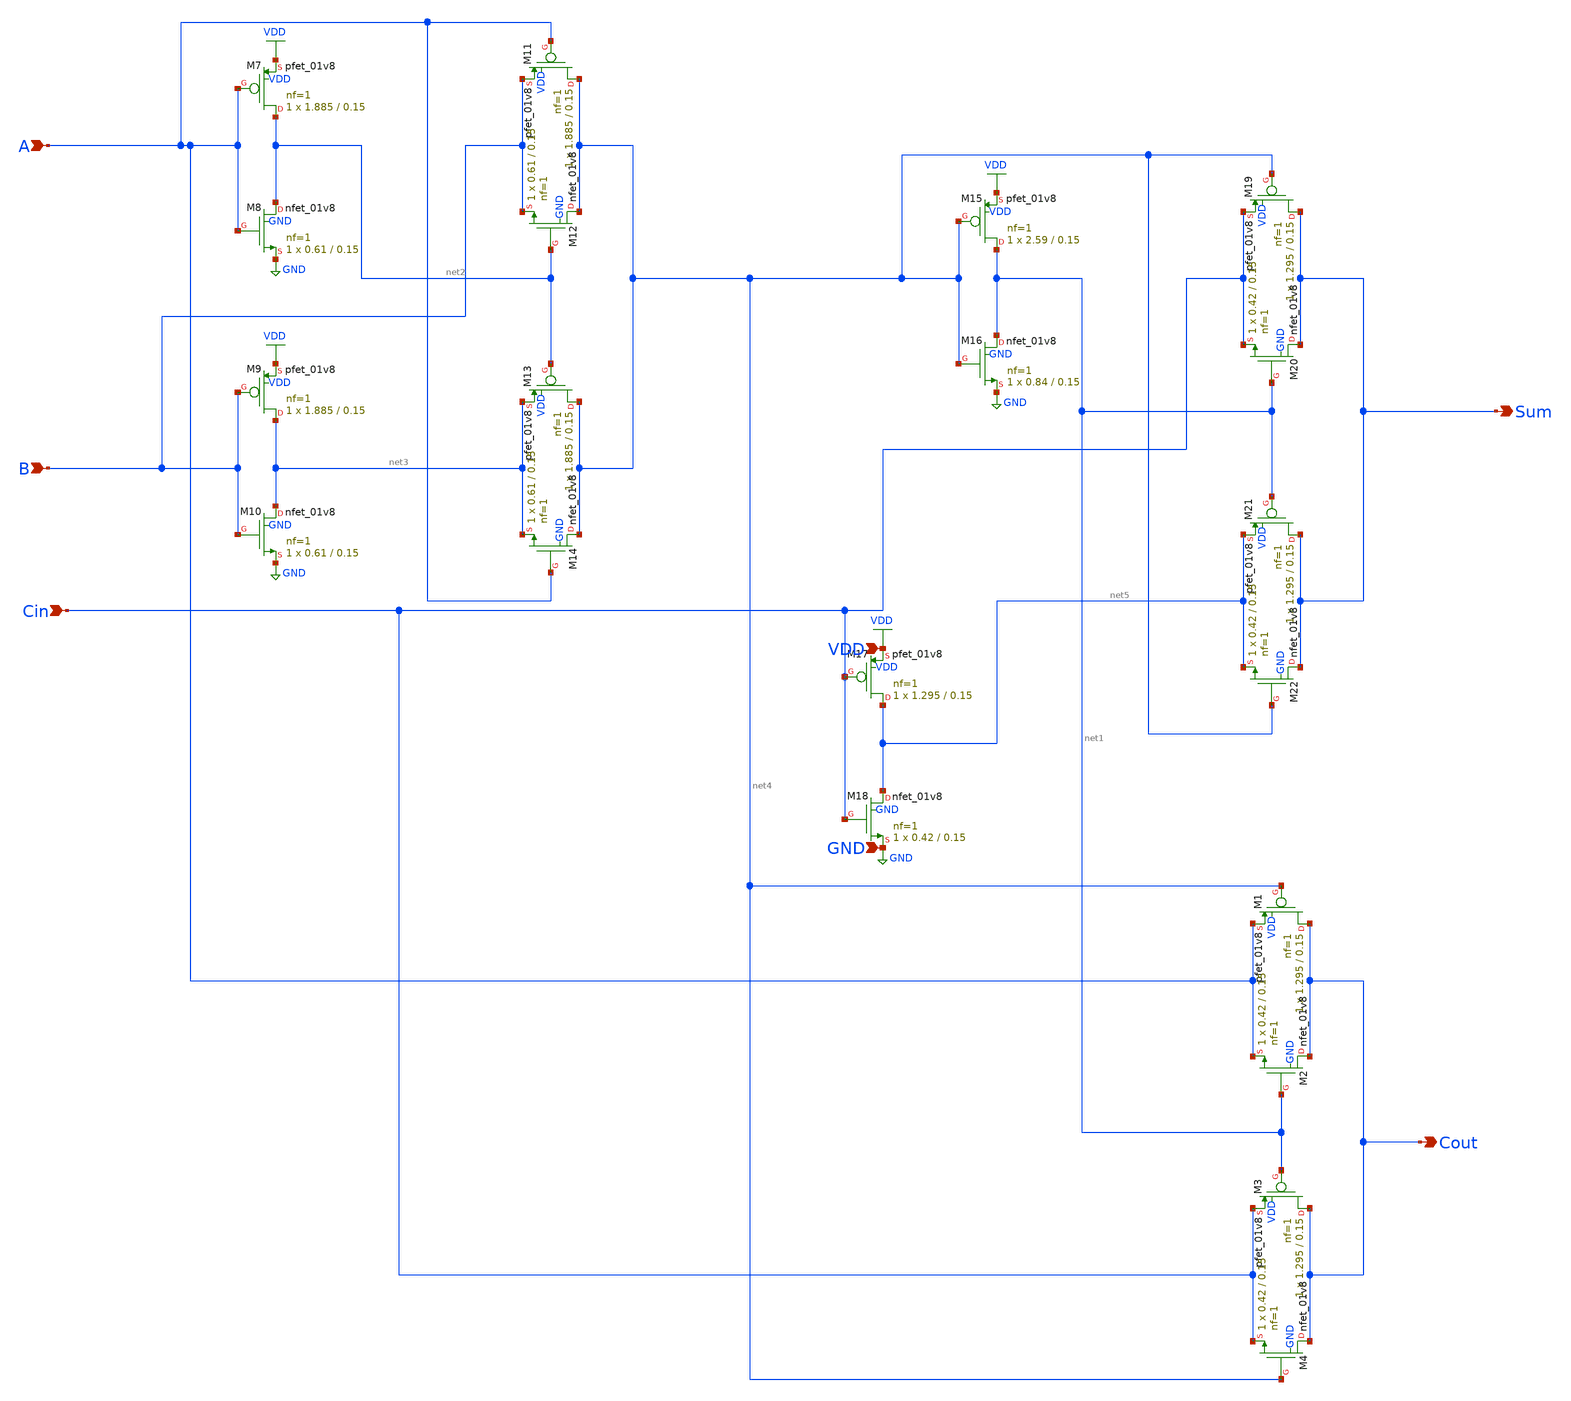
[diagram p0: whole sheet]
** sch_path: transmission_gate/schematic/fulladder.sch
**.subckt fulladder Cout A B Cin Sum VDD GND
*.opin Cout
*.ipin A
*.ipin B
*.ipin Cin
*.opin Sum
*.ipin VDD
*.ipin GND
XM1 Cout net4 A VDD sky130_fd_pr__pfet_01v8 L=0.15 W=1.295 nf=1 ad='int((1 + 1)/2) * 1.295 / 1 * 0.29'
+ as='int((1 + 2)/2) * 1.295 / 1 * 0.29' pd='2*int((1 + 1)/2) * (1.295 / 1 + 0.29)' ps='2*int((1 + 2)/2) * (1.295 / 1 + 0.29)'
+ nrd='0.29 / 1.295 ' nrs='0.29 / 1.295 ' sa=0 sb=0 sd=0 mult=1 m=1
XM2 Cout net1 A GND sky130_fd_pr__nfet_01v8 L=0.15 W=0.42 nf=1 ad='int((1 + 1)/2) * 0.42 / 1 * 0.29'
+ as='int((1 + 2)/2) * 0.42 / 1 * 0.29' pd='2*int((1 + 1)/2) * (0.42 / 1 + 0.29)' ps='2*int((1 + 2)/2) * (0.42 / 1 + 0.29)'
+ nrd='0.29 / 0.42 ' nrs='0.29 / 0.42 ' sa=0 sb=0 sd=0 mult=1 m=1
XM3 Cout net1 Cin VDD sky130_fd_pr__pfet_01v8 L=0.15 W=1.295 nf=1 ad='int((1 + 1)/2) * 1.295 / 1 * 0.29'
+ as='int((1 + 2)/2) * 1.295 / 1 * 0.29' pd='2*int((1 + 1)/2) * (1.295 / 1 + 0.29)' ps='2*int((1 + 2)/2) * (1.295 / 1 + 0.29)'
+ nrd='0.29 / 1.295 ' nrs='0.29 / 1.295 ' sa=0 sb=0 sd=0 mult=1 m=1
XM4 Cout net4 Cin GND sky130_fd_pr__nfet_01v8 L=0.15 W=0.42 nf=1 ad='int((1 + 1)/2) * 0.42 / 1 * 0.29'
+ as='int((1 + 2)/2) * 0.42 / 1 * 0.29' pd='2*int((1 + 1)/2) * (0.42 / 1 + 0.29)' ps='2*int((1 + 2)/2) * (0.42 / 1 + 0.29)'
+ nrd='0.29 / 0.42 ' nrs='0.29 / 0.42 ' sa=0 sb=0 sd=0 mult=1 m=1
XM7 net2 A VDD VDD sky130_fd_pr__pfet_01v8 L=0.15 W=1.885 nf=1 ad='int((1 + 1)/2) * 1.885 / 1 * 0.29'
+ as='int((1 + 2)/2) * 1.885 / 1 * 0.29' pd='2*int((1 + 1)/2) * (1.885 / 1 + 0.29)' ps='2*int((1 + 2)/2) * (1.885 / 1 + 0.29)'
+ nrd='0.29 / 1.885 ' nrs='0.29 / 1.885 ' sa=0 sb=0 sd=0 mult=1 m=1
XM8 net2 A GND GND sky130_fd_pr__nfet_01v8 L=0.15 W=0.61 nf=1 ad='int((1 + 1)/2) * 0.61 / 1 * 0.29' as='int((1 + 2)/2) * 0.61 / 1 * 0.29'
+ pd='2*int((1 + 1)/2) * (0.61 / 1 + 0.29)' ps='2*int((1 + 2)/2) * (0.61 / 1 + 0.29)' nrd='0.29 / 0.61 '
+ nrs='0.29 / 0.61 ' sa=0 sb=0 sd=0 mult=1 m=1
XM9 net3 B VDD VDD sky130_fd_pr__pfet_01v8 L=0.15 W=1.885 nf=1 ad='int((1 + 1)/2) * 1.885 / 1 * 0.29'
+ as='int((1 + 2)/2) * 1.885 / 1 * 0.29' pd='2*int((1 + 1)/2) * (1.885 / 1 + 0.29)' ps='2*int((1 + 2)/2) * (1.885 / 1 + 0.29)'
+ nrd='0.29 / 1.885 ' nrs='0.29 / 1.885 ' sa=0 sb=0 sd=0 mult=1 m=1
XM10 net3 B GND GND sky130_fd_pr__nfet_01v8 L=0.15 W=0.61 nf=1 ad='int((1 + 1)/2) * 0.61 / 1 * 0.29'
+ as='int((1 + 2)/2) * 0.61 / 1 * 0.29' pd='2*int((1 + 1)/2) * (0.61 / 1 + 0.29)' ps='2*int((1 + 2)/2) * (0.61 / 1 + 0.29)'
+ nrd='0.29 / 0.61 ' nrs='0.29 / 0.61 ' sa=0 sb=0 sd=0 mult=1 m=1
XM11 net4 A B VDD sky130_fd_pr__pfet_01v8 L=0.15 W=1.885 nf=1 ad='int((1 + 1)/2) * 1.885 / 1 * 0.29'
+ as='int((1 + 2)/2) * 1.885 / 1 * 0.29' pd='2*int((1 + 1)/2) * (1.885 / 1 + 0.29)' ps='2*int((1 + 2)/2) * (1.885 / 1 + 0.29)'
+ nrd='0.29 / 1.885 ' nrs='0.29 / 1.885 ' sa=0 sb=0 sd=0 mult=1 m=1
XM12 net4 net2 B GND sky130_fd_pr__nfet_01v8 L=0.15 W=0.61 nf=1 ad='int((1 + 1)/2) * 0.61 / 1 * 0.29'
+ as='int((1 + 2)/2) * 0.61 / 1 * 0.29' pd='2*int((1 + 1)/2) * (0.61 / 1 + 0.29)' ps='2*int((1 + 2)/2) * (0.61 / 1 + 0.29)'
+ nrd='0.29 / 0.61 ' nrs='0.29 / 0.61 ' sa=0 sb=0 sd=0 mult=1 m=1
XM13 net4 net2 net3 VDD sky130_fd_pr__pfet_01v8 L=0.15 W=1.885 nf=1 ad='int((1 + 1)/2) * 1.885 / 1 * 0.29'
+ as='int((1 + 2)/2) * 1.885 / 1 * 0.29' pd='2*int((1 + 1)/2) * (1.885 / 1 + 0.29)' ps='2*int((1 + 2)/2) * (1.885 / 1 + 0.29)'
+ nrd='0.29 / 1.885 ' nrs='0.29 / 1.885 ' sa=0 sb=0 sd=0 mult=1 m=1
XM14 net4 A net3 GND sky130_fd_pr__nfet_01v8 L=0.15 W=0.61 nf=1 ad='int((1 + 1)/2) * 0.61 / 1 * 0.29'
+ as='int((1 + 2)/2) * 0.61 / 1 * 0.29' pd='2*int((1 + 1)/2) * (0.61 / 1 + 0.29)' ps='2*int((1 + 2)/2) * (0.61 / 1 + 0.29)'
+ nrd='0.29 / 0.61 ' nrs='0.29 / 0.61 ' sa=0 sb=0 sd=0 mult=1 m=1
XM15 net1 net4 VDD VDD sky130_fd_pr__pfet_01v8 L=0.15 W=2.59 nf=1 ad='int((1 + 1)/2) * 2.59 / 1 * 0.29'
+ as='int((1 + 2)/2) * 2.59 / 1 * 0.29' pd='2*int((1 + 1)/2) * (2.59 / 1 + 0.29)' ps='2*int((1 + 2)/2) * (2.59 / 1 + 0.29)'
+ nrd='0.29 / 2.59 ' nrs='0.29 / 2.59 ' sa=0 sb=0 sd=0 mult=1 m=1
XM16 net1 net4 GND GND sky130_fd_pr__nfet_01v8 L=0.15 W=0.84 nf=1 ad='int((1 + 1)/2) * 0.84 / 1 * 0.29'
+ as='int((1 + 2)/2) * 0.84 / 1 * 0.29' pd='2*int((1 + 1)/2) * (0.84 / 1 + 0.29)' ps='2*int((1 + 2)/2) * (0.84 / 1 + 0.29)'
+ nrd='0.29 / 0.84 ' nrs='0.29 / 0.84 ' sa=0 sb=0 sd=0 mult=1 m=1
XM17 net5 Cin VDD VDD sky130_fd_pr__pfet_01v8 L=0.15 W=1.295 nf=1 ad='int((1 + 1)/2) * 1.295 / 1 * 0.29'
+ as='int((1 + 2)/2) * 1.295 / 1 * 0.29' pd='2*int((1 + 1)/2) * (1.295 / 1 + 0.29)' ps='2*int((1 + 2)/2) * (1.295 / 1 + 0.29)'
+ nrd='0.29 / 1.295 ' nrs='0.29 / 1.295 ' sa=0 sb=0 sd=0 mult=1 m=1
XM18 net5 Cin GND GND sky130_fd_pr__nfet_01v8 L=0.15 W=0.42 nf=1 ad='int((1 + 1)/2) * 0.42 / 1 * 0.29'
+ as='int((1 + 2)/2) * 0.42 / 1 * 0.29' pd='2*int((1 + 1)/2) * (0.42 / 1 + 0.29)' ps='2*int((1 + 2)/2) * (0.42 / 1 + 0.29)'
+ nrd='0.29 / 0.42 ' nrs='0.29 / 0.42 ' sa=0 sb=0 sd=0 mult=1 m=1
XM19 Sum net4 Cin VDD sky130_fd_pr__pfet_01v8 L=0.15 W=1.295 nf=1 ad='int((1 + 1)/2) * 1.295 / 1 * 0.29'
+ as='int((1 + 2)/2) * 1.295 / 1 * 0.29' pd='2*int((1 + 1)/2) * (1.295 / 1 + 0.29)' ps='2*int((1 + 2)/2) * (1.295 / 1 + 0.29)'
+ nrd='0.29 / 1.295 ' nrs='0.29 / 1.295 ' sa=0 sb=0 sd=0 mult=1 m=1
XM20 Sum net1 Cin GND sky130_fd_pr__nfet_01v8 L=0.15 W=0.42 nf=1 ad='int((1 + 1)/2) * 0.42 / 1 * 0.29'
+ as='int((1 + 2)/2) * 0.42 / 1 * 0.29' pd='2*int((1 + 1)/2) * (0.42 / 1 + 0.29)' ps='2*int((1 + 2)/2) * (0.42 / 1 + 0.29)'
+ nrd='0.29 / 0.42 ' nrs='0.29 / 0.42 ' sa=0 sb=0 sd=0 mult=1 m=1
XM21 Sum net1 net5 VDD sky130_fd_pr__pfet_01v8 L=0.15 W=1.295 nf=1 ad='int((1 + 1)/2) * 1.295 / 1 * 0.29'
+ as='int((1 + 2)/2) * 1.295 / 1 * 0.29' pd='2*int((1 + 1)/2) * (1.295 / 1 + 0.29)' ps='2*int((1 + 2)/2) * (1.295 / 1 + 0.29)'
+ nrd='0.29 / 1.295 ' nrs='0.29 / 1.295 ' sa=0 sb=0 sd=0 mult=1 m=1
XM22 Sum net4 net5 GND sky130_fd_pr__nfet_01v8 L=0.15 W=0.42 nf=1 ad='int((1 + 1)/2) * 0.42 / 1 * 0.29'
+ as='int((1 + 2)/2) * 0.42 / 1 * 0.29' pd='2*int((1 + 1)/2) * (0.42 / 1 + 0.29)' ps='2*int((1 + 2)/2) * (0.42 / 1 + 0.29)'
+ nrd='0.29 / 0.42 ' nrs='0.29 / 0.42 ' sa=0 sb=0 sd=0 mult=1 m=1
**.ends
.GLOBAL GND
.GLOBAL VDD
.end
